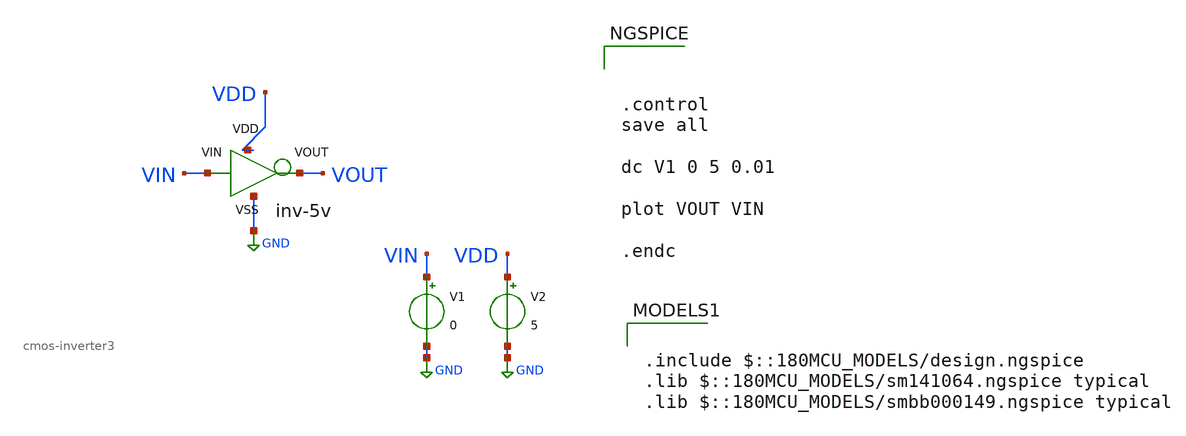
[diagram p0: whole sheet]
** sch_path: week01_mosfet_cmos/tugas2_cmos_inverter/cmos-inverter3-tb.sch
**.subckt cmos-inverter3-tb
x1 VDD VIN VOUT GND cmos-inverter3
V1 VIN GND 0
V2 VDD GND 5
**** begin user architecture code



.control
save all

dc V1 0 5 0.01

plot VOUT VIN

.endc



.include $::180MCU_MODELS/design.ngspice
.lib $::180MCU_MODELS/sm141064.ngspice typical
.lib $::180MCU_MODELS/smbb000149.ngspice typical

**** end user architecture code
**.ends

* expanding   symbol:  cmos-inverter3.sym # of pins=4
** sym_path: week01_mosfet_cmos/tugas2_cmos_inverter/cmos-inverter3.sym
** sch_path: week01_mosfet_cmos/tugas2_cmos_inverter/cmos-inverter3.sch
.subckt cmos-inverter3 VDD VIN VOUT VSS
*.iopin VDD
*.iopin VSS
*.ipin VIN
*.opin VOUT
XM1 VOUT VIN VDD net1 pfet_05v0 L=0.50u W=0.30u nf=1 ad='int((nf+1)/2) * W/nf * 0.18u' as='int((nf+2)/2) * W/nf * 0.18u'
+ pd='2*int((nf+1)/2) * (W/nf + 0.18u)' ps='2*int((nf+2)/2) * (W/nf + 0.18u)' nrd='0.18u / W' nrs='0.18u / W'
+ sa=0 sb=0 sd=0 m=1
XM2 VOUT VIN VSS net2 nfet_05v0 L=0.60u W=0.30u nf=1 ad='int((nf+1)/2) * W/nf * 0.18u' as='int((nf+2)/2) * W/nf * 0.18u'
+ pd='2*int((nf+1)/2) * (W/nf + 0.18u)' ps='2*int((nf+2)/2) * (W/nf + 0.18u)' nrd='0.18u / W' nrs='0.18u / W'
+ sa=0 sb=0 sd=0 m=1
.ends

.GLOBAL GND
.end
